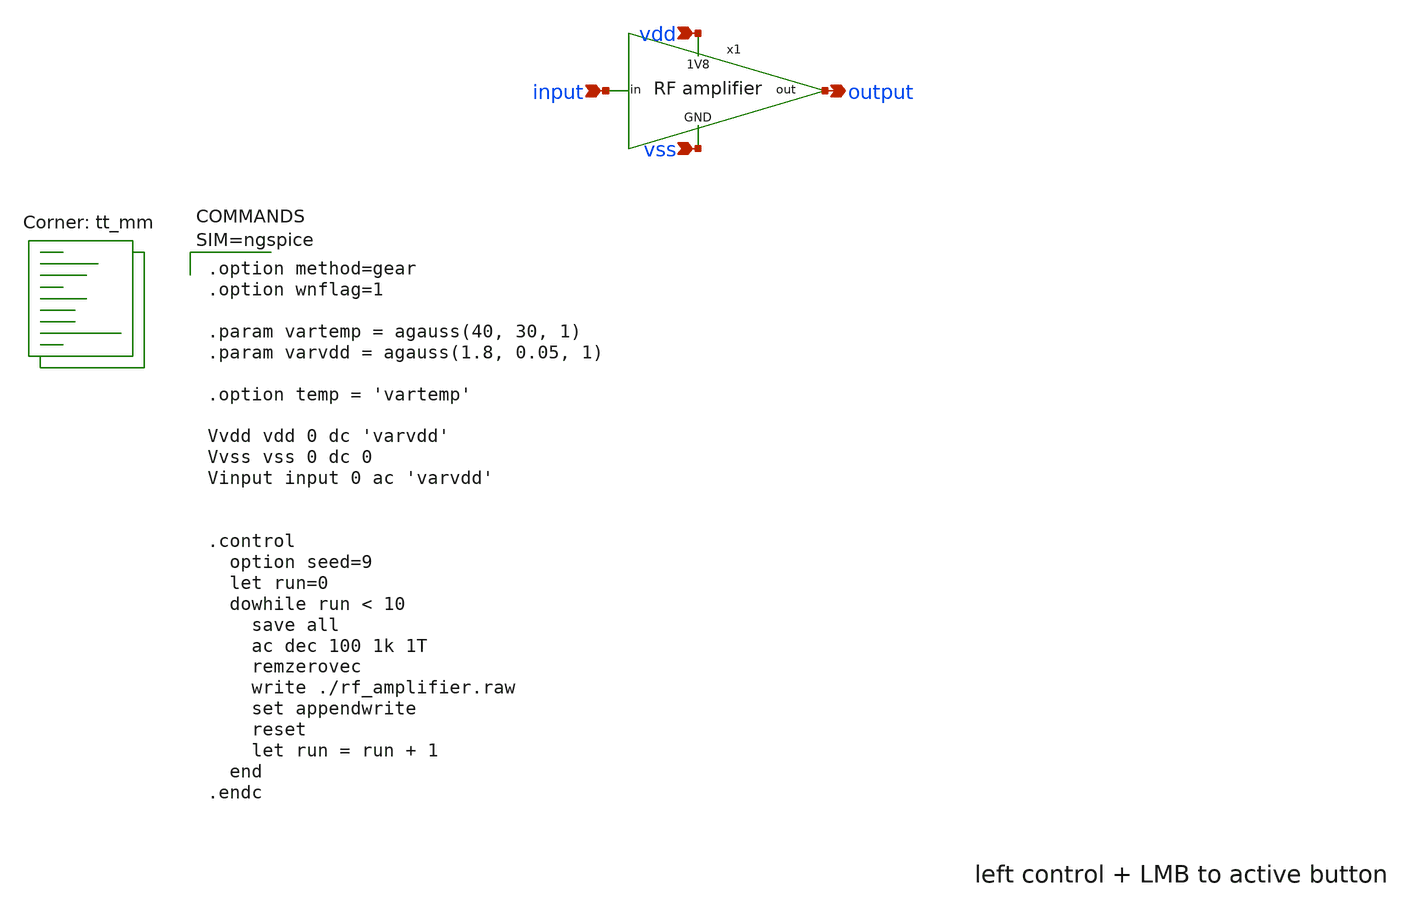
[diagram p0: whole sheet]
** sch_path: tests/rf_amplifier.sch
**.subckt rf_amplifier input output vdd vss
*.ipin input
*.opin output
*.ipin vdd
*.ipin vss
x1 vdd input output vss rf_amplifier
**** begin user architecture code
.lib $::SKYWATER_MODELS/sky130.lib.spice tt_mm


.option method=gear
.option wnflag=1

.param vartemp = agauss(40, 30, 1)
.param varvdd = agauss(1.8, 0.05, 1)

.option temp = 'vartemp'

Vvdd vdd 0 dc 'varvdd'
Vvss vss 0 dc 0
Vinput input 0 ac 'varvdd'


.control
  option seed=9
  let run=0
  dowhile run < 10
    save all
    ac dec 100 1k 1T
    remzerovec
    write ./rf_amplifier.raw
    set appendwrite
    reset
    let run = run + 1
  end
.endc


**** end user architecture code
**.ends

* expanding   symbol:  ./rf_amplifier.sym # of pins=4
** sym_path: schematic/rf_amplifier.sym
** sch_path: schematic/rf_amplifier.sch
.subckt rf_amplifier 1V8 in out GND
*.ipin in
*.opin out
*.ipin GND
*.ipin 1V8
* noconn 1V8
* noconn GND
R1 out in 0 m=1
.ends

.end
